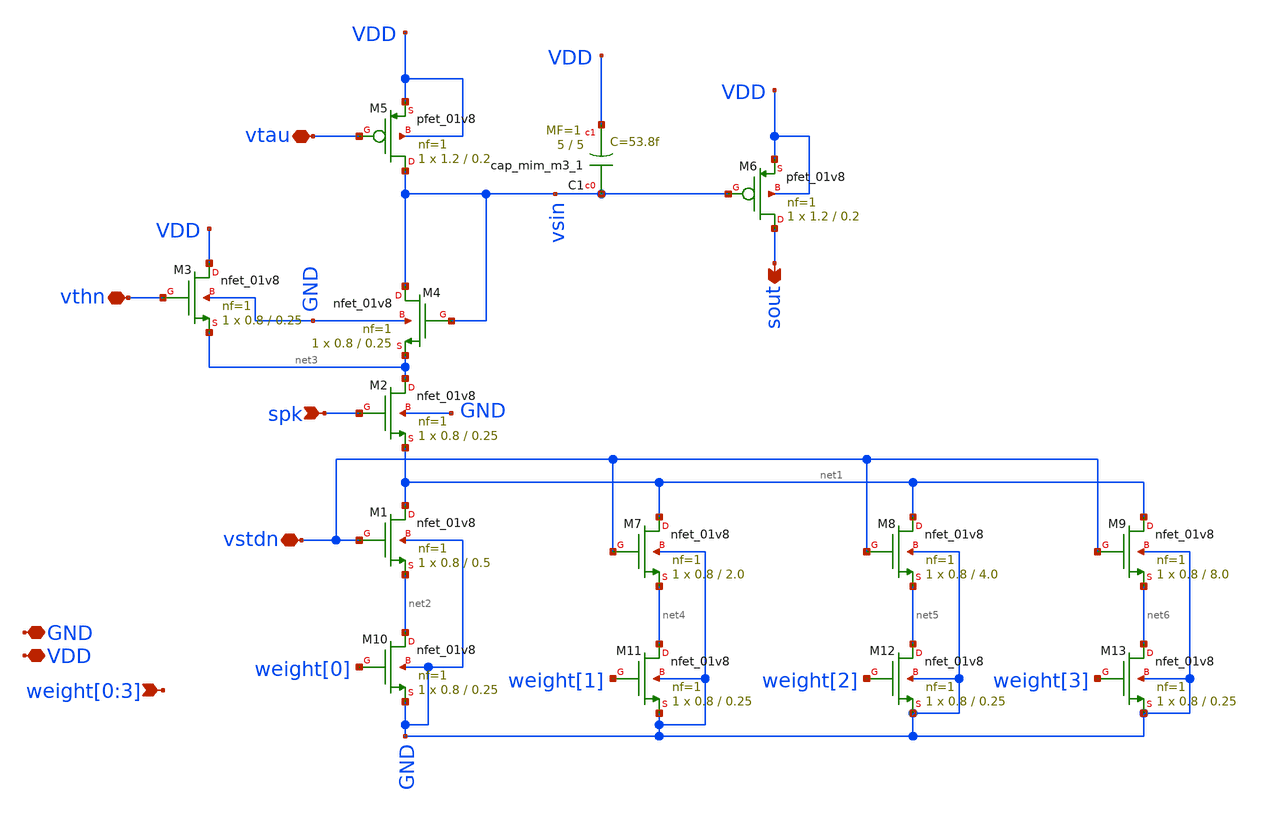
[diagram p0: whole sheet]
** sch_path: design/xschem/dpi_syn_exc_4bit_fc.sch
**.subckt dpi_syn_exc_4bit_fc GND VDD vtau vstdn spk sout vthn
*+ weight[0],weight[1],weight[2],weight[3]
*.iopin GND
*.iopin VDD
*.iopin vtau
*.iopin vstdn
*.ipin spk
*.opin sout
*.iopin vthn
*.ipin weight[0],weight[1],weight[2],weight[3]
XM2 net3 spk net1 GND sky130_fd_pr__nfet_01v8 L=0.25 W=0.8 nf=1 ad='int((nf+1)/2) * W/nf * 0.29' as='int((nf+2)/2) * W/nf * 0.29'
+ pd='2*int((nf+1)/2) * (W/nf + 0.29)' ps='2*int((nf+2)/2) * (W/nf + 0.29)' nrd='0.29 / W' nrs='0.29 / W'
+ sa=0 sb=0 sd=0 mult=1 m=1
XC1 vsin VDD sky130_fd_pr__cap_mim_m3_1 W=5 L=5 MF=1 m=1
XM5 vsin vtau VDD VDD sky130_fd_pr__pfet_01v8 L=0.2 W=1.2 nf=1 ad='int((nf+1)/2) * W/nf * 0.29' as='int((nf+2)/2) * W/nf * 0.29'
+ pd='2*int((nf+1)/2) * (W/nf + 0.29)' ps='2*int((nf+2)/2) * (W/nf + 0.29)' nrd='0.29 / W' nrs='0.29 / W'
+ sa=0 sb=0 sd=0 mult=1 m=1
XM6 sout vsin VDD VDD sky130_fd_pr__pfet_01v8 L=0.2 W=1.2 nf=1 ad='int((nf+1)/2) * W/nf * 0.29' as='int((nf+2)/2) * W/nf * 0.29'
+ pd='2*int((nf+1)/2) * (W/nf + 0.29)' ps='2*int((nf+2)/2) * (W/nf + 0.29)' nrd='0.29 / W' nrs='0.29 / W'
+ sa=0 sb=0 sd=0 mult=1 m=1
XM1 net1 vstdn net2 GND sky130_fd_pr__nfet_01v8 L=0.5 W=0.8 nf=1 ad='int((nf+1)/2) * W/nf * 0.29' as='int((nf+2)/2) * W/nf * 0.29'
+ pd='2*int((nf+1)/2) * (W/nf + 0.29)' ps='2*int((nf+2)/2) * (W/nf + 0.29)' nrd='0.29 / W' nrs='0.29 / W'
+ sa=0 sb=0 sd=0 mult=1 m=1
XM4 vsin vsin net3 GND sky130_fd_pr__nfet_01v8 L=0.25 W=0.8 nf=1 ad='int((nf+1)/2) * W/nf * 0.29' as='int((nf+2)/2) * W/nf * 0.29'
+ pd='2*int((nf+1)/2) * (W/nf + 0.29)' ps='2*int((nf+2)/2) * (W/nf + 0.29)' nrd='0.29 / W' nrs='0.29 / W'
+ sa=0 sb=0 sd=0 mult=1 m=1
XM3 VDD vthn net3 GND sky130_fd_pr__nfet_01v8 L=0.25 W=0.8 nf=1 ad='int((nf+1)/2) * W/nf * 0.29' as='int((nf+2)/2) * W/nf * 0.29'
+ pd='2*int((nf+1)/2) * (W/nf + 0.29)' ps='2*int((nf+2)/2) * (W/nf + 0.29)' nrd='0.29 / W' nrs='0.29 / W'
+ sa=0 sb=0 sd=0 mult=1 m=1
XM7 net1 vstdn net4 GND sky130_fd_pr__nfet_01v8 L=2.0 W=0.8 nf=1 ad='int((nf+1)/2) * W/nf * 0.29' as='int((nf+2)/2) * W/nf * 0.29'
+ pd='2*int((nf+1)/2) * (W/nf + 0.29)' ps='2*int((nf+2)/2) * (W/nf + 0.29)' nrd='0.29 / W' nrs='0.29 / W'
+ sa=0 sb=0 sd=0 mult=1 m=1
XM8 net1 vstdn net5 GND sky130_fd_pr__nfet_01v8 L=4.0 W=0.8 nf=1 ad='int((nf+1)/2) * W/nf * 0.29' as='int((nf+2)/2) * W/nf * 0.29'
+ pd='2*int((nf+1)/2) * (W/nf + 0.29)' ps='2*int((nf+2)/2) * (W/nf + 0.29)' nrd='0.29 / W' nrs='0.29 / W'
+ sa=0 sb=0 sd=0 mult=1 m=1
XM9 net1 vstdn net6 GND sky130_fd_pr__nfet_01v8 L=8.0 W=0.8 nf=1 ad='int((nf+1)/2) * W/nf * 0.29' as='int((nf+2)/2) * W/nf * 0.29'
+ pd='2*int((nf+1)/2) * (W/nf + 0.29)' ps='2*int((nf+2)/2) * (W/nf + 0.29)' nrd='0.29 / W' nrs='0.29 / W'
+ sa=0 sb=0 sd=0 mult=1 m=1
XM10 net2 weight[0] GND GND sky130_fd_pr__nfet_01v8 L=0.25 W=0.8 nf=1 ad='int((nf+1)/2) * W/nf * 0.29'
+ as='int((nf+2)/2) * W/nf * 0.29' pd='2*int((nf+1)/2) * (W/nf + 0.29)' ps='2*int((nf+2)/2) * (W/nf + 0.29)'
+ nrd='0.29 / W' nrs='0.29 / W' sa=0 sb=0 sd=0 mult=1 m=1
XM11 net4 weight[1] GND GND sky130_fd_pr__nfet_01v8 L=0.25 W=0.8 nf=1 ad='int((nf+1)/2) * W/nf * 0.29'
+ as='int((nf+2)/2) * W/nf * 0.29' pd='2*int((nf+1)/2) * (W/nf + 0.29)' ps='2*int((nf+2)/2) * (W/nf + 0.29)'
+ nrd='0.29 / W' nrs='0.29 / W' sa=0 sb=0 sd=0 mult=1 m=1
XM12 net5 weight[2] GND GND sky130_fd_pr__nfet_01v8 L=0.25 W=0.8 nf=1 ad='int((nf+1)/2) * W/nf * 0.29'
+ as='int((nf+2)/2) * W/nf * 0.29' pd='2*int((nf+1)/2) * (W/nf + 0.29)' ps='2*int((nf+2)/2) * (W/nf + 0.29)'
+ nrd='0.29 / W' nrs='0.29 / W' sa=0 sb=0 sd=0 mult=1 m=1
XM13 net6 weight[3] GND GND sky130_fd_pr__nfet_01v8 L=0.25 W=0.8 nf=1 ad='int((nf+1)/2) * W/nf * 0.29'
+ as='int((nf+2)/2) * W/nf * 0.29' pd='2*int((nf+1)/2) * (W/nf + 0.29)' ps='2*int((nf+2)/2) * (W/nf + 0.29)'
+ nrd='0.29 / W' nrs='0.29 / W' sa=0 sb=0 sd=0 mult=1 m=1
**.ends
.end
